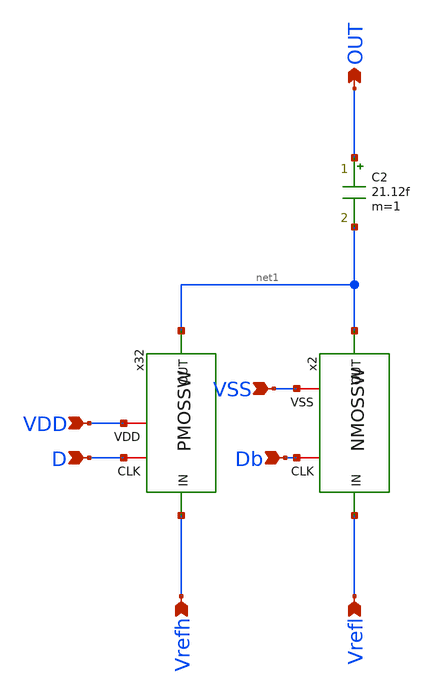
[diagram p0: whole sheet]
** sch_path: Cunit.sch
**.subckt Cunit VSS VDD D Db Vrefh Vrefl OUT
*.ipin VSS
*.ipin VDD
*.ipin D
*.ipin Db
*.ipin Vrefh
*.ipin Vrefl
*.opin OUT
C2 OUT net1 21.12f m=1
x2 Db VSS net1 Vrefl NMOSSW
x32 D net1 Vrefh VDD PMOSSW
**.ends

* expanding   symbol:  NMOSSW.sym # of pins=4
** sym_path: NMOSSW.sym
** sch_path: NMOSSW.sch
.subckt NMOSSW CLK VSS OUT IN
*.ipin IN
*.iopin VSS
*.opin OUT
*.iopin CLK
M1 OUT CLK IN VSS nch w=0.7u l=0.35u as=0 ps=0 ad=0 pd=0 m=1
.ends


* expanding   symbol:  PMOSSW.sym # of pins=4
** sym_path: PMOSSW.sym
** sch_path: PMOSSW.sch
.subckt PMOSSW CLK OUT IN VDD
*.ipin IN
*.opin OUT
*.iopin VDD
*.iopin CLK
M5 OUT CLK IN VDD pch w=0.7u l=0.35u as=0 ps=0 ad=0 pd=0 m=1
.ends

.end
